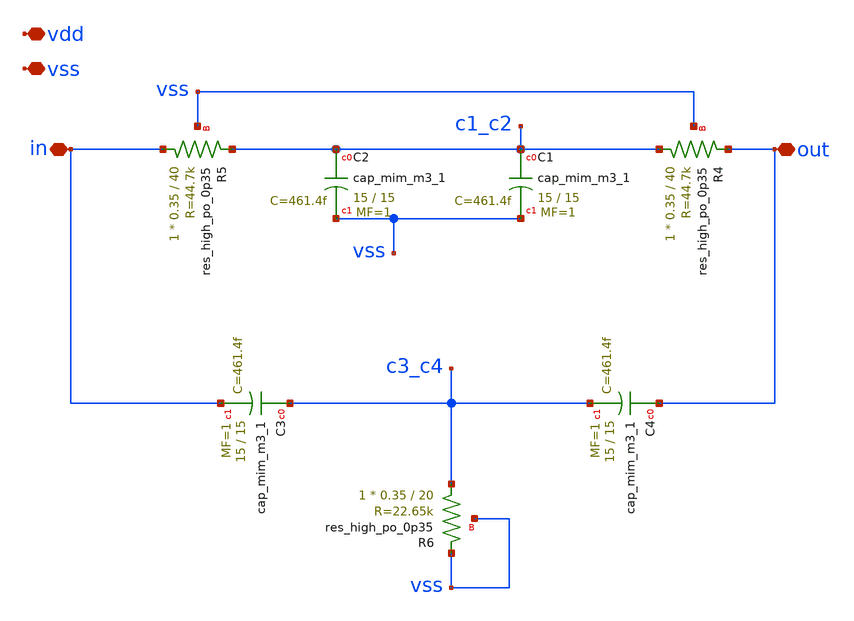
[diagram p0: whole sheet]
** sch_path: xschem/twin_tee.sch
**.subckt twin_tee vdd vss in out
*.iopin vdd
*.iopin vss
*.iopin in
*.iopin out
XR4 c1_c2 out vss sky130_fd_pr__res_high_po_0p35 L=40 mult=1 m=1
XC1 c1_c2 vss sky130_fd_pr__cap_mim_m3_1 W=15 L=15 MF=1 m=1
XC2 c1_c2 vss sky130_fd_pr__cap_mim_m3_1 W=15 L=15 MF=1 m=1
XR5 in c1_c2 vss sky130_fd_pr__res_high_po_0p35 L=40 mult=1 m=1
XC3 c3_c4 in sky130_fd_pr__cap_mim_m3_1 W=15 L=15 MF=1 m=1
XC4 out c3_c4 sky130_fd_pr__cap_mim_m3_1 W=15 L=15 MF=1 m=1
XR6 c3_c4 vss vss sky130_fd_pr__res_high_po_0p35 L=20 mult=1 m=1
**.ends
.end
